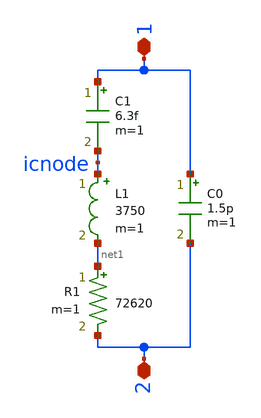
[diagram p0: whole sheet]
** sch_path: xschem/xtal_abs_060.sch
**.subckt xtal_abs_060 1 2
*.iopin 1
*.iopin 2
L1 icnode net1 3750 m=1
C1 1 icnode 6.3f m=1
C0 1 2 1.5p m=1
R1 net1 2 72620 m=1
**.ends
.end
